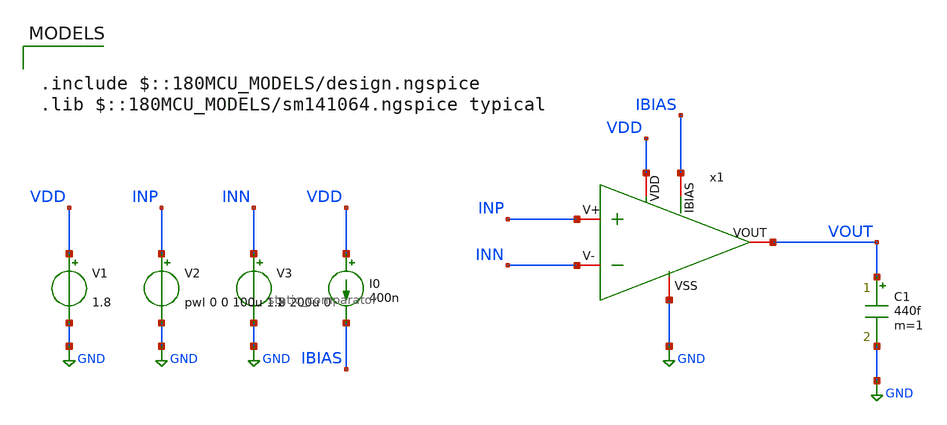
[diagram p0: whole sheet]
** sch_path: designs/static_comparator/xschem/static_comparator_tb_tran.sch
**.subckt static_comparator_tb_tran
V1 VDD GND 1.8
V2 INP GND pwl 0 0 100u 1.8 200u 0
C1 VOUT GND 440f m=1
V3 INN GND 1
I0 VDD IBIAS 400n
x1 VDD IBIAS GND INP INN VOUT static_comparator
**** begin user architecture code

.include $::180MCU_MODELS/design.ngspice
.lib $::180MCU_MODELS/sm141064.ngspice typical




.control
save all

** Simulación transitoria
tran 1u 200u

setplot tran1
let vin  = v(INP)
let vref = v(INN)
let vout = v(VOUT)
plot vout vin vref

write comparator_tb_tran.raw
.endc


**** end user architecture code
**.ends
.GLOBAL GND
.end
